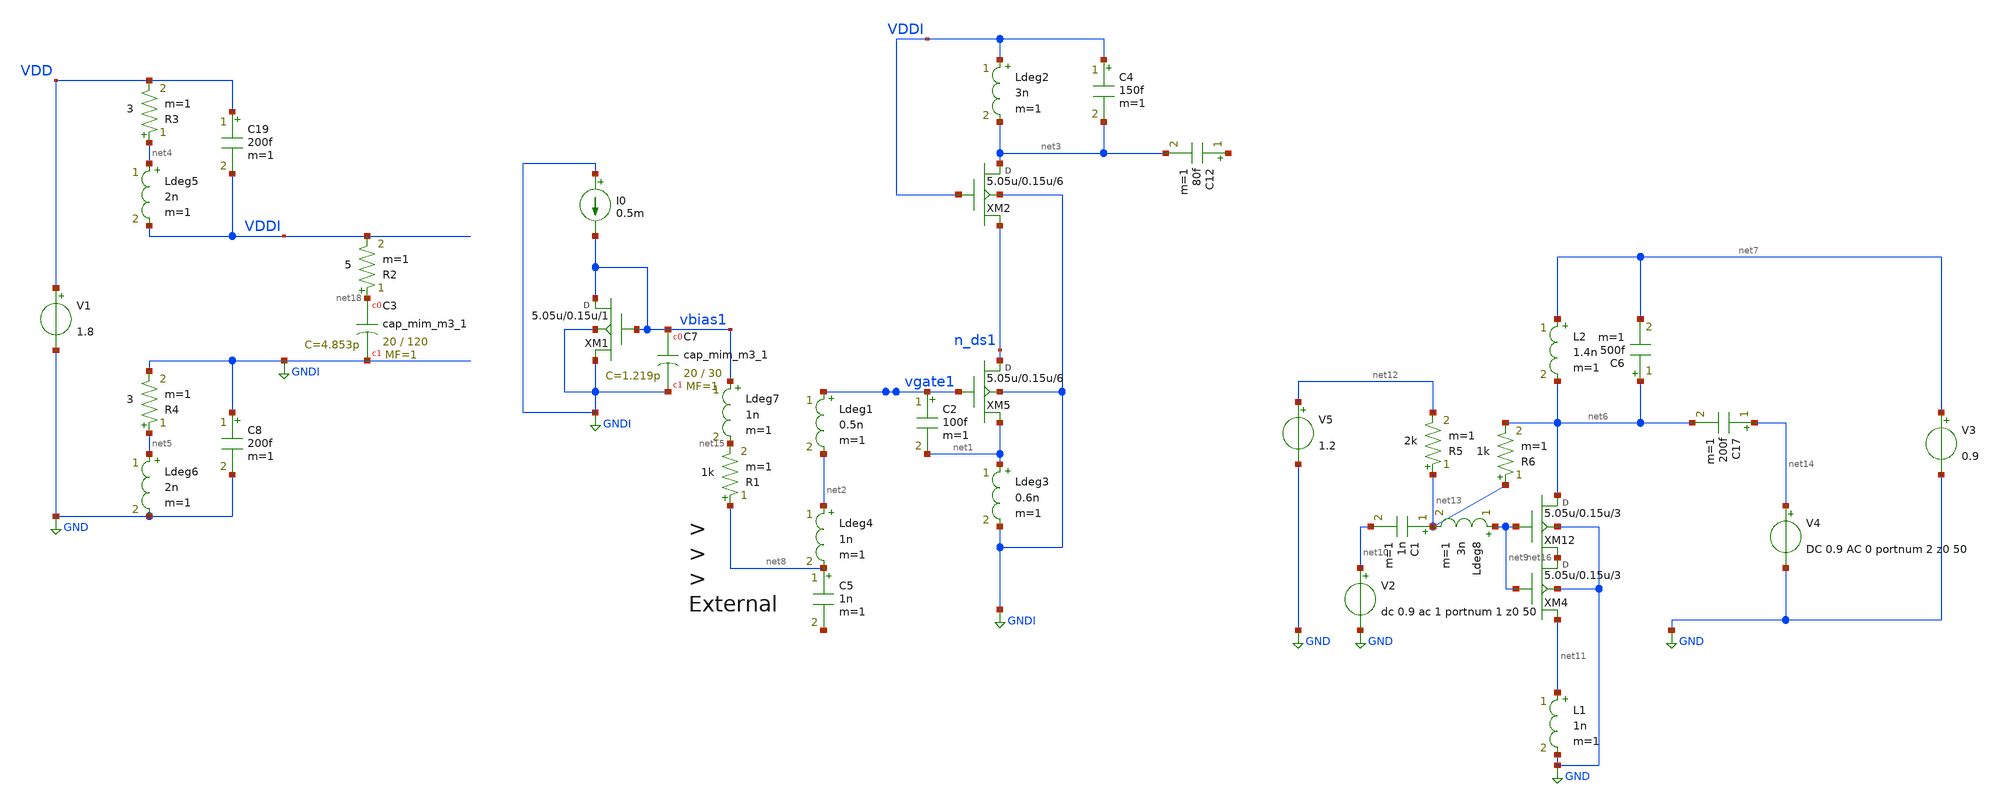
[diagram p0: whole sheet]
** sch_path: xschem/LNA5_with_output_buf.sch
**.subckt LNA5_with_output_buf
V1 VDD GND 1.8
V2 net10 GND dc 0.9 ac 1 portnum 1 z0 50
Ldeg3 net1 GNDI 0.6n m=1
C2 vgate1 net1 100f m=1
R1 net8 net15 1k m=1
Ldeg1 vgate1 net2 0.5n m=1
I0 GNDI vbias1 0.5m
Ldeg2 VDDI net3 3n m=1
XM5 n_ds1 vgate1 net1 GNDI sky130_fd_pr__rf_nfet_01v8_bM04W5p00L0p15_ext w=5.05u l=0.15u m=6
XM1 vbias1 vbias1 GNDI GNDI sky130_fd_pr__rf_nfet_01v8_bM04W5p00L0p15_ext w=5.05u l=0.15u m=1
XM2 net3 VDDI n_ds1 GNDI sky130_fd_pr__rf_nfet_01v8_bM04W5p00L0p15_ext w=5.05u l=0.15u m=6
XC7 vbias1 GNDI sky130_fd_pr__cap_mim_m3_1 W=20 L=30 MF=1 m=1
Ldeg5 net4 VDDI 2n m=1
R3 net4 VDD 3 m=1
Ldeg6 net5 GND 2n m=1
R4 net5 GNDI 3 m=1
XM12 net6 net9 net16 GND sky130_fd_pr__rf_nfet_01v8_bM04W5p00L0p15_ext w=5.05u l=0.15u m=3
V4 net14 GND DC 0.9 AC 0 portnum 2 z0 50
L1 net11 GND 1n m=1
C17 net14 net6 200f m=1
L2 net7 net6 1.4n m=1
C12 net17 net3 80f m=1
XC3 net18 GNDI sky130_fd_pr__cap_mim_m3_1 W=20 L=120 MF=1 m=1
C8 GNDI GND 200f m=1
C19 VDD VDDI 200f m=1
R2 net18 VDDI 5 m=1
C5 net8 net19 1n m=1
C4 VDDI net3 150f m=1
Ldeg4 net2 net8 1n m=1
Ldeg7 vbias1 net15 1n m=1
Ldeg8 net9 net13 3n m=1
R5 net13 net12 2k m=1
V3 net7 GND 0.9
XM4 net16 net9 net11 GND sky130_fd_pr__rf_nfet_01v8_bM04W5p00L0p15_ext w=5.05u l=0.15u m=3
V5 net12 GND 1.2
C1 net13 net10 1n m=1
C6 net6 net7 500f m=1
R6 net13 net6 1k m=1
**** begin user architecture code
.lib $::SKYWATER_MODELS/sky130.lib.spice tt
* .include $::PDKPATH/libs.ref/sky130_fd_sc_hvl/spice/sky130_fd_sc_hvl.spice



.subckt sky130_fd_pr__rf_nfet_01v8_bM04W5p00L0p15_ext DRAIN GATE SOURCE SUBSTRATE
X0 DRAIN GATE SOURCE SUBSTRATE sky130_fd_pr__nfet_01v8 ad=2.828e+12p pd=2.132e+07u as=4.242e+12p
+ ps=3.198e+07u w=5.05e+06u l=150000u
X1 SOURCE SUBSTRATE SUBSTRATE SUBSTRATE sky130_fd_pr__nfet_01v8 ad=0p pd=0u as=3.03e+12p
+ ps=2.14e+07u w=5.05e+06u l=150000u
X2 SOURCE GATE DRAIN SUBSTRATE sky130_fd_pr__nfet_01v8 ad=0p pd=0u as=0p ps=0u w=5.05e+06u l=150000u
X3 DRAIN GATE SOURCE SUBSTRATE sky130_fd_pr__nfet_01v8 ad=0p pd=0u as=0p ps=0u w=5.05e+06u l=150000u
X4 SUBSTRATE SUBSTRATE SOURCE SUBSTRATE sky130_fd_pr__nfet_01v8 ad=0p pd=0u as=0p ps=0u w=5.05e+06u
+ l=150000u
X5 SOURCE GATE DRAIN SUBSTRATE sky130_fd_pr__nfet_01v8 ad=0p pd=0u as=0p ps=0u w=5.05e+06u l=150000u
.ends
.sp dec 1000 0.1e9 10e9 1
* .ac dec 1000 0.01e9 100e9
.control
run
display
let z11=50*(1+s_1_1)/(1-s_1_1)
let z22=50*(1+s_2_2)/(1-s_2_2)
let S11 = S_1_1
let S21 = S_2_1
let S12 = S_1_2
let S22 = S_2_2

* Stability
let delta=S11*S22-S12*S21
let K    = (1-mag(S11)^2-mag(S22)^2+mag(delta)^2)/(2*mag(S12*S21))
let mu   = (1-mag(S11)^2)/(mag(S22-conj(S11)*delta)+mag(S21*S12))
* plot real(z11) real(z22)
* plot imag(z11) imag(z22)
plot db(S_1_1) db(S_2_2) db(S_2_1)

plot K
plot mag(delta)
plot mu
.endc


**** end user architecture code
**.ends
.GLOBAL GND
.GLOBAL GNDI
.end
